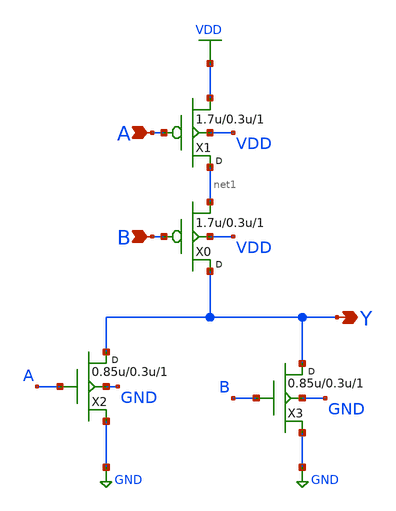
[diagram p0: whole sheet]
** sch_path: gf180mcu_osu_sc_gp12t3v3/cells/nor2/gf180mcu_osu_sc_gp12t3v3__nor2_1.sch
**.subckt gf180mcu_osu_sc_gp12t3v3__nor2_1 A B Y
*.ipin A
*.ipin B
*.opin Y
X1 net1 A VDD VDD pfet_03p3 w=1.7u l=0.3u m=1
X0 Y B net1 VDD pfet_03p3 w=1.7u l=0.3u m=1
X2 Y A GND GND nfet_03p3 w=0.85u l=0.3u m=1
X3 Y B GND GND nfet_03p3 w=0.85u l=0.3u m=1
**.ends
.GLOBAL VDD
.GLOBAL GND
.end
